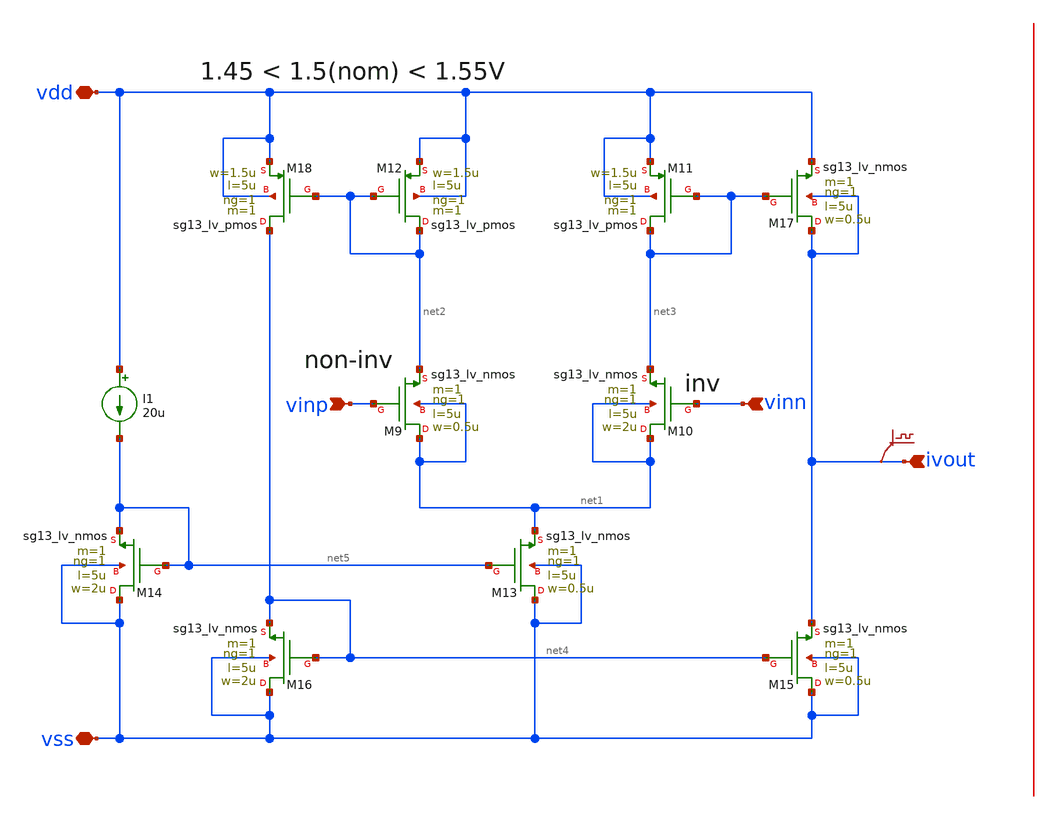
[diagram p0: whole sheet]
** sch_path: 3_Real_Cir/10_Real_Cir/test_Real_Cir/Improved/improved_5t_ota_v2_A.sch
* Copyright 2023 IHP PDK Authors
* Licensed under the Apache License, Version 2.0 (the "License");
* you may not use this file except in compliance with the License.
* You may obtain a copy of the License at
* https://www.apache.org/licenses/LICENSE-2.0
* Unless required by applicable law or agreed to in writing, software
* distributed under the License is distributed on an "AS IS" BASIS,
* WITHOUT WARRANTIES OR CONDITIONS OF ANY KIND, either express or implied.
* See the License for the specific language governing permissions and
* limitations under the License.
* Copyright 2024 IHP PDK Authors
**.subckt improved_5t_ota_v2_A ivout vdd vinp vinn vss
*.ipin ivout
*.iopin vdd
*.ipin vinp
*.ipin vinn
*.iopin vss
XM11 net3 net3 vdd vdd sg13_lv_pmos w=1.5u l=5u ng=1 m=1 mm_ok=1
XM12 net2 net2 vdd vdd sg13_lv_pmos w=1.5u l=5u ng=1 m=1 mm_ok=1
XM13 vss net5 net1 vss sg13_lv_nmos w=0.5u l=5u ng=1 m=1 mm_ok=1
XM16 vss net4 net4 vss sg13_lv_nmos w=2u l=5u ng=1 m=1 mm_ok=1
XM9 net1 vinp net2 net1 sg13_lv_nmos w=0.5u l=5u ng=1 m=1 mm_ok=1
XM17 ivout net3 vdd ivout sg13_lv_nmos w=0.5u l=5u ng=1 m=1 mm_ok=1
XM15 vss net4 ivout vss sg13_lv_nmos w=0.5u l=5u ng=1 m=1 mm_ok=1
XM18 net4 net2 vdd vdd sg13_lv_pmos w=1.5u l=5u ng=1 m=1 mm_ok=1
XM14 vss net5 net5 vss sg13_lv_nmos w=2u l=5u ng=1 m=1 mm_ok=1
XM10 net1 vinn net3 net1 sg13_lv_nmos w=2u l=5u ng=1 m=1 mm_ok=1
.save v(ivout)
I1 vdd net5 20u
**.ends
.end
